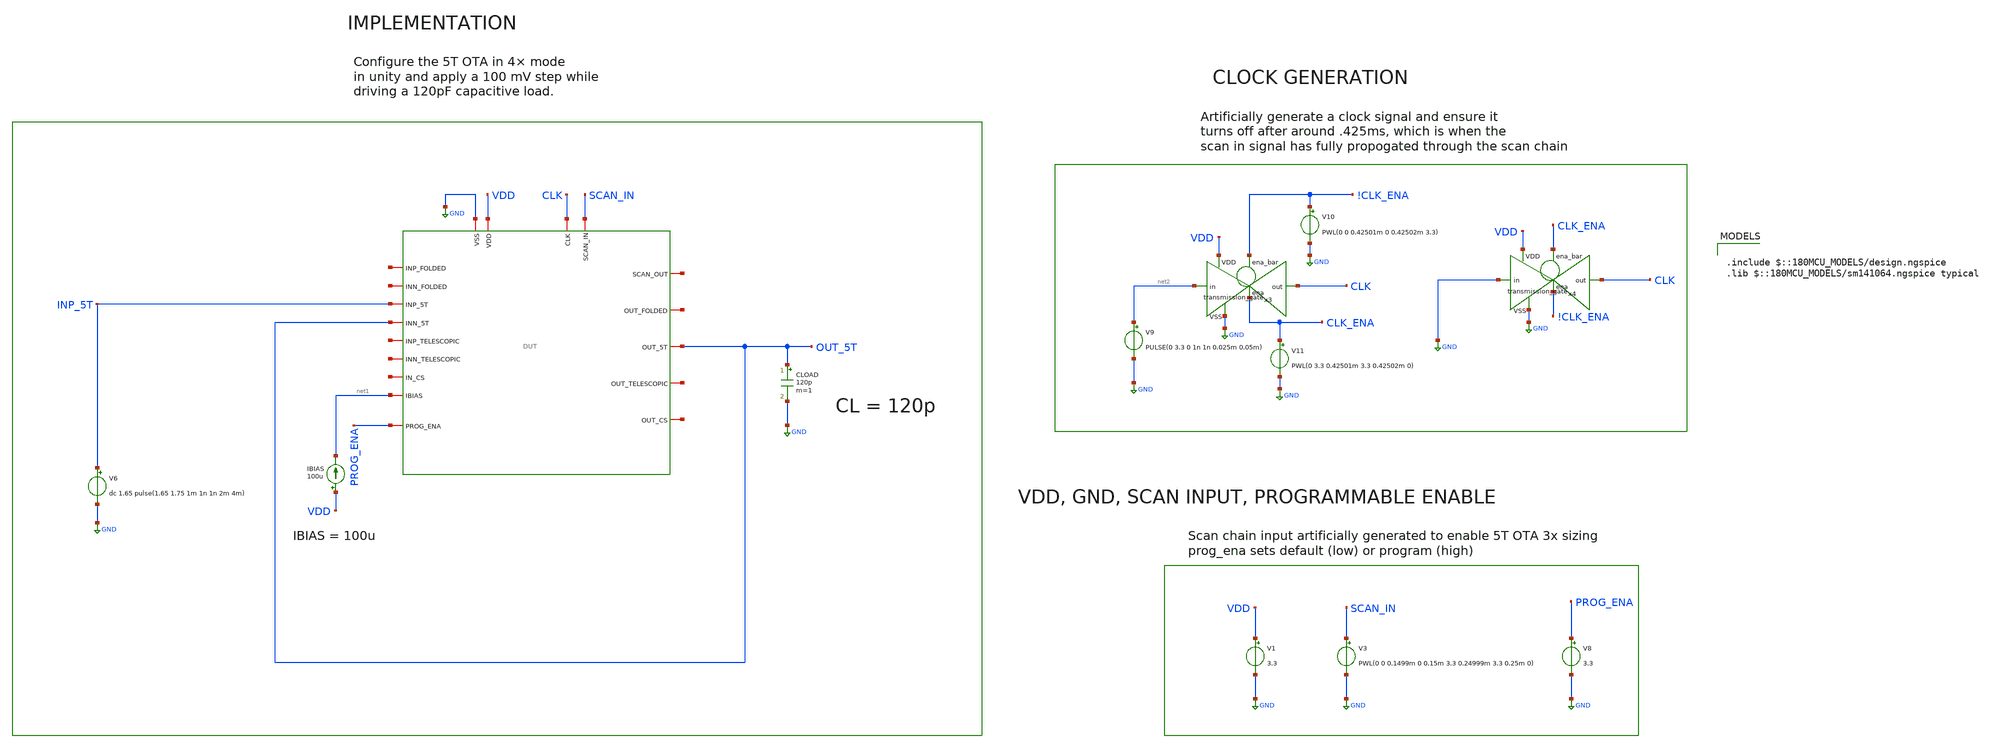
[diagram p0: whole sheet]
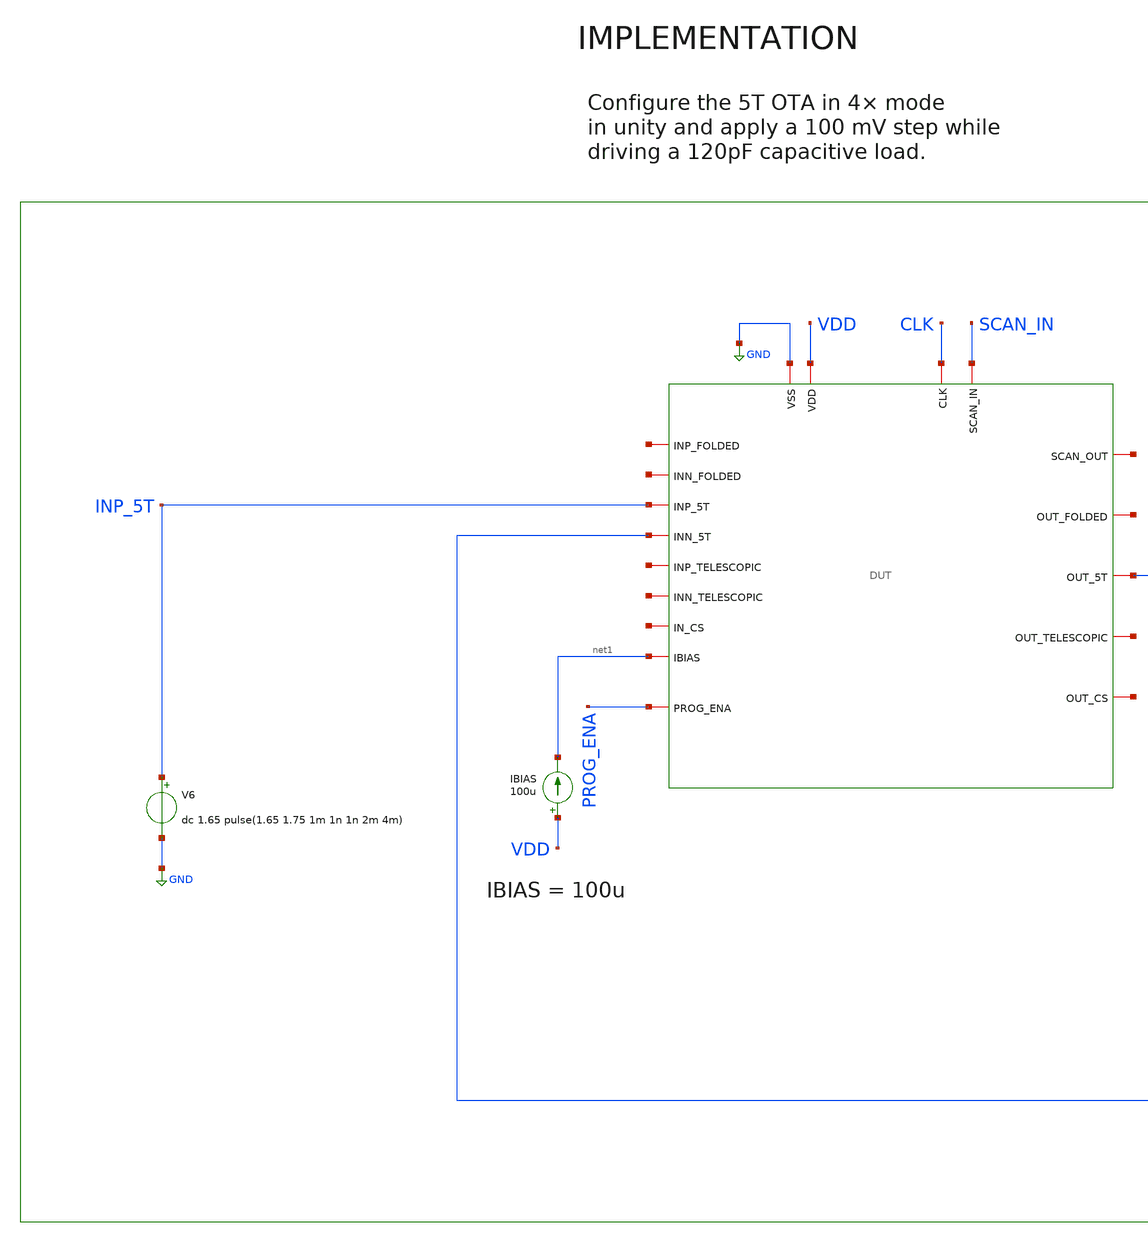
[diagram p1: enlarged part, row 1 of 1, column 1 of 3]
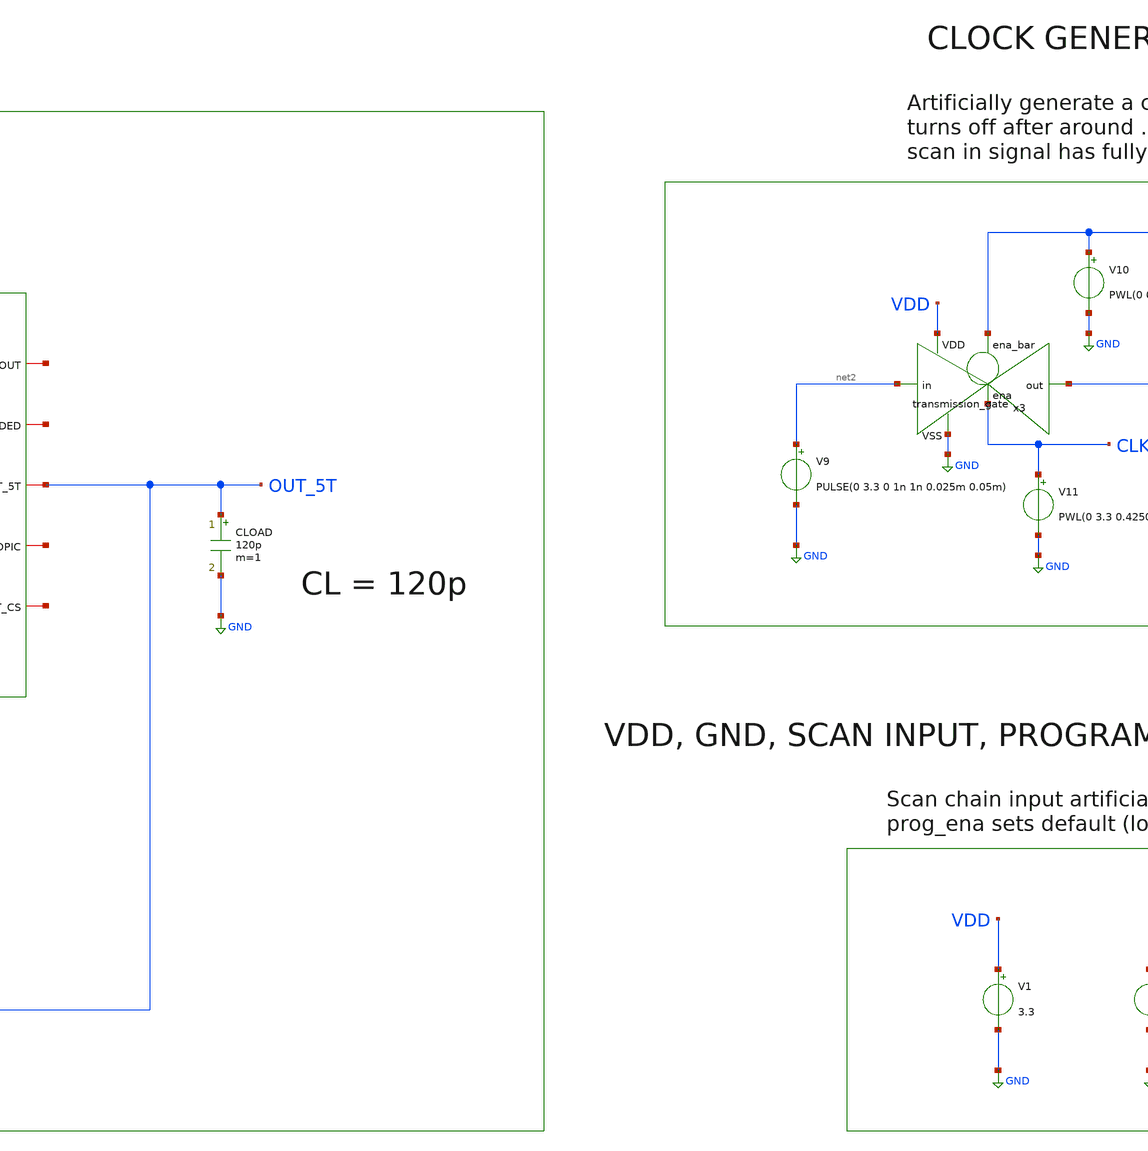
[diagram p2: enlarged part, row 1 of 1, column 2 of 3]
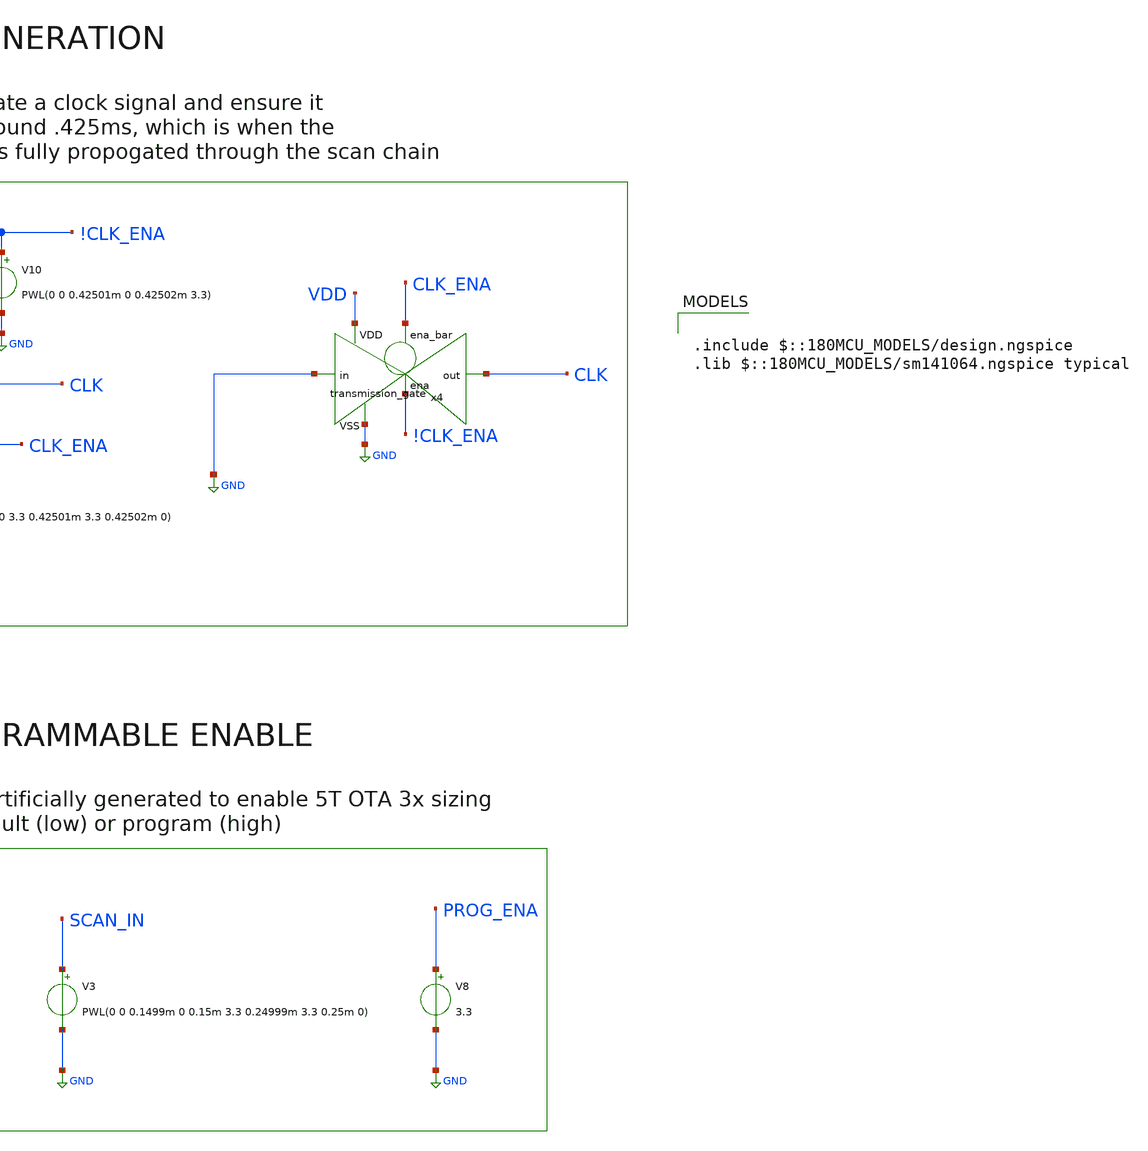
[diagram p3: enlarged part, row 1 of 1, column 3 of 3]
** sch_path: designs/libs/verification/ota_5t/4x_sizing/5t_4x_step_response_tb.sch
**.subckt 5t_4x_step_response_tb
V3 SCAN_IN GND PWL(0 0 0.1499m 0 0.15m 3.3 0.24999m 3.3 0.25m 0)
V1 VDD GND 3.3
IBIAS VDD net1 100u
CLOAD OUT_5T GND 120p m=1
x1 CLK net3 SCAN_IN GND VDD net4 net5 OUT_5T net1 net6 INP_5T OUT_5T net7 net8 net9 net10 net11
+ PROG_ENA DUT
V8 PROG_ENA GND 3.3
V9 net2 GND PULSE(0 3.3 0 1n 1n 0.025m 0.05m)
x3 !CLK_ENA VDD CLK net2 GND CLK_ENA transmission_gate
V10 !CLK_ENA GND PWL(0 0 0.42501m 0 0.42502m 3.3)
V11 CLK_ENA GND PWL(0 3.3 0.42501m 3.3 0.42502m 0)
x4 CLK_ENA VDD CLK GND GND !CLK_ENA transmission_gate
V6 INP_5T GND dc 1.65 pulse(1.65 1.75 1m 1n 1n 2m 4m)
**** begin user architecture code

.include $::180MCU_MODELS/design.ngspice
.lib $::180MCU_MODELS/sm141064.ngspice typical



.control
tran 1u 5m

plot v(out_5T) v(inp_5T)

meas tran v_before find v(out_5T) at=0.99m
meas tran v_after find v(out_5T) at=2.5m

let delta = v_after - v_before
let t20_val = v_before + 0.2 * delta
let t80_val = v_before + 0.8 * delta

meas tran t_20 when v(out_5T) = t20_val rise = 1
meas tran t_80 when v(out_5T) = t80_val rise = 1
let sr_rise = delta / (t_80 - t_20)
print sr_rise

meas tran t_20f when v(out_5T) = t80_val fall = 1
meas tran t_80f when v(out_5T) = t20_val fall = 1
let sr_fall = delta / (t_80f - t_20f)
print sr_fall

meas tran vpeak max v(out_5T) from=1m to=3m
let overshoot = (vpeak - v_after) / delta * 100
print overshoot

meas tran t_settle when v(out_5T) = v_after td = 1m rise = 1
let settling = t_settle - 1m
print settling

print v_before v_after delta
.endc


**** end user architecture code
**.ends
.GLOBAL GND
.end
